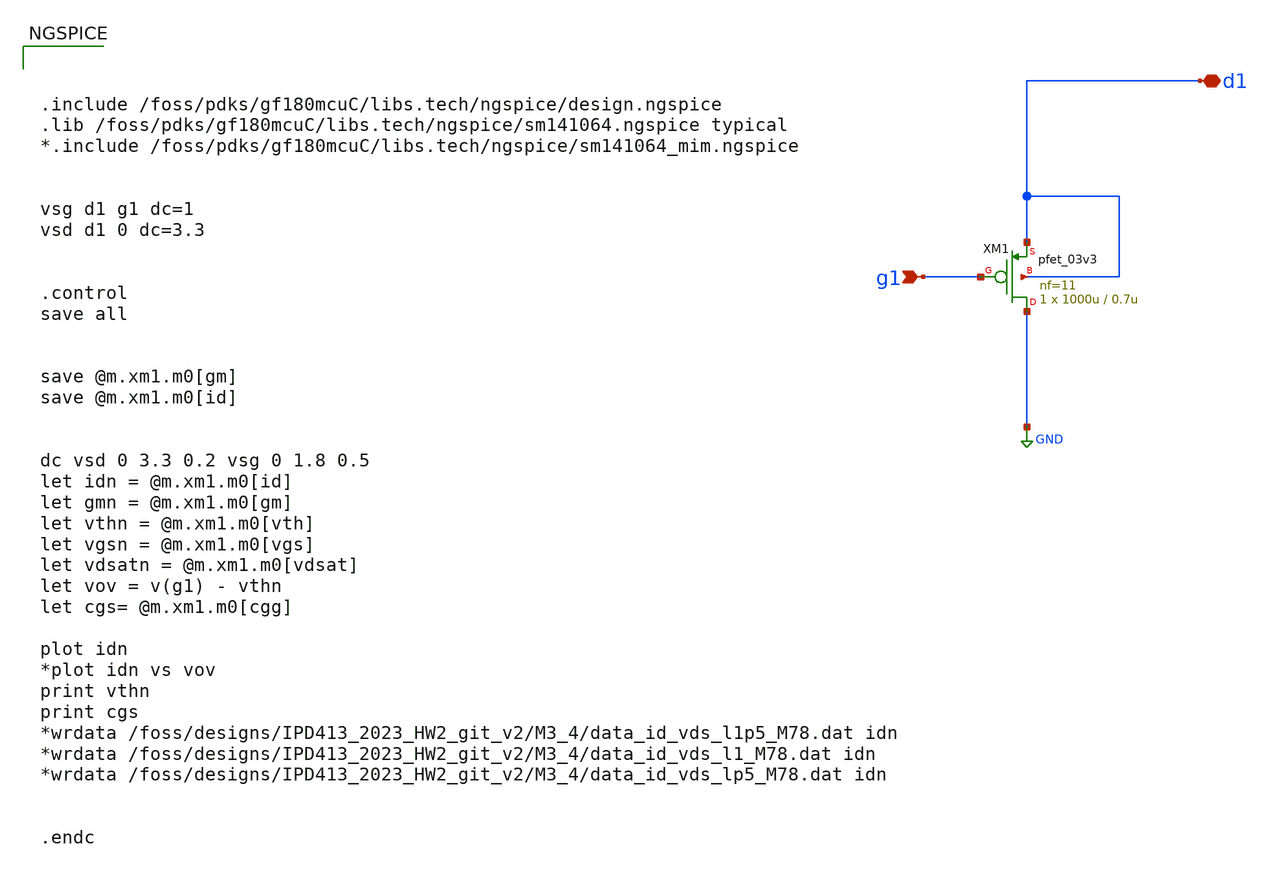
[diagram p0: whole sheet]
** sch_path: Xschem/Caracteristica_disp/pmos_gf180_3p3V.sch
**.subckt pmos_gf180_3p3V g1 d1
*.ipin g1
*.iopin d1
XM1 GND g1 d1 d1 pfet_03v3 L=0.7u W=1000u nf=11 ad='int((nf+1)/2) * W/nf * 0.18u' as='int((nf+2)/2) * W/nf * 0.18u'
+ pd='2*int((nf+1)/2) * (W/nf + 0.18u)' ps='2*int((nf+2)/2) * (W/nf + 0.18u)' nrd='0.18u / W' nrs='0.18u / W'
+ sa=0 sb=0 sd=0 m=1
**** begin user architecture code



.include /foss/pdks/gf180mcuC/libs.tech/ngspice/design.ngspice
.lib /foss/pdks/gf180mcuC/libs.tech/ngspice/sm141064.ngspice typical
*.include /foss/pdks/gf180mcuC/libs.tech/ngspice/sm141064_mim.ngspice


vsg d1 g1 dc=1
vsd d1 0 dc=3.3


.control
save all


save @m.xm1.m0[gm]
save @m.xm1.m0[id]


dc vsd 0 3.3 0.2 vsg 0 1.8 0.5
let idn = @m.xm1.m0[id]
let gmn = @m.xm1.m0[gm]
let vthn = @m.xm1.m0[vth]
let vgsn = @m.xm1.m0[vgs]
let vdsatn = @m.xm1.m0[vdsat]
let vov = v(g1) - vthn
let cgs= @m.xm1.m0[cgg]

plot idn
*plot idn vs vov
print vthn
print cgs
*wrdata /foss/designs/IPD413_2023_HW2_git_v2/M3_4/data_id_vds_l1p5_M78.dat idn
*wrdata /foss/designs/IPD413_2023_HW2_git_v2/M3_4/data_id_vds_l1_M78.dat idn
*wrdata /foss/designs/IPD413_2023_HW2_git_v2/M3_4/data_id_vds_lp5_M78.dat idn


.endc


**** end user architecture code
**.ends
.GLOBAL GND
.end
